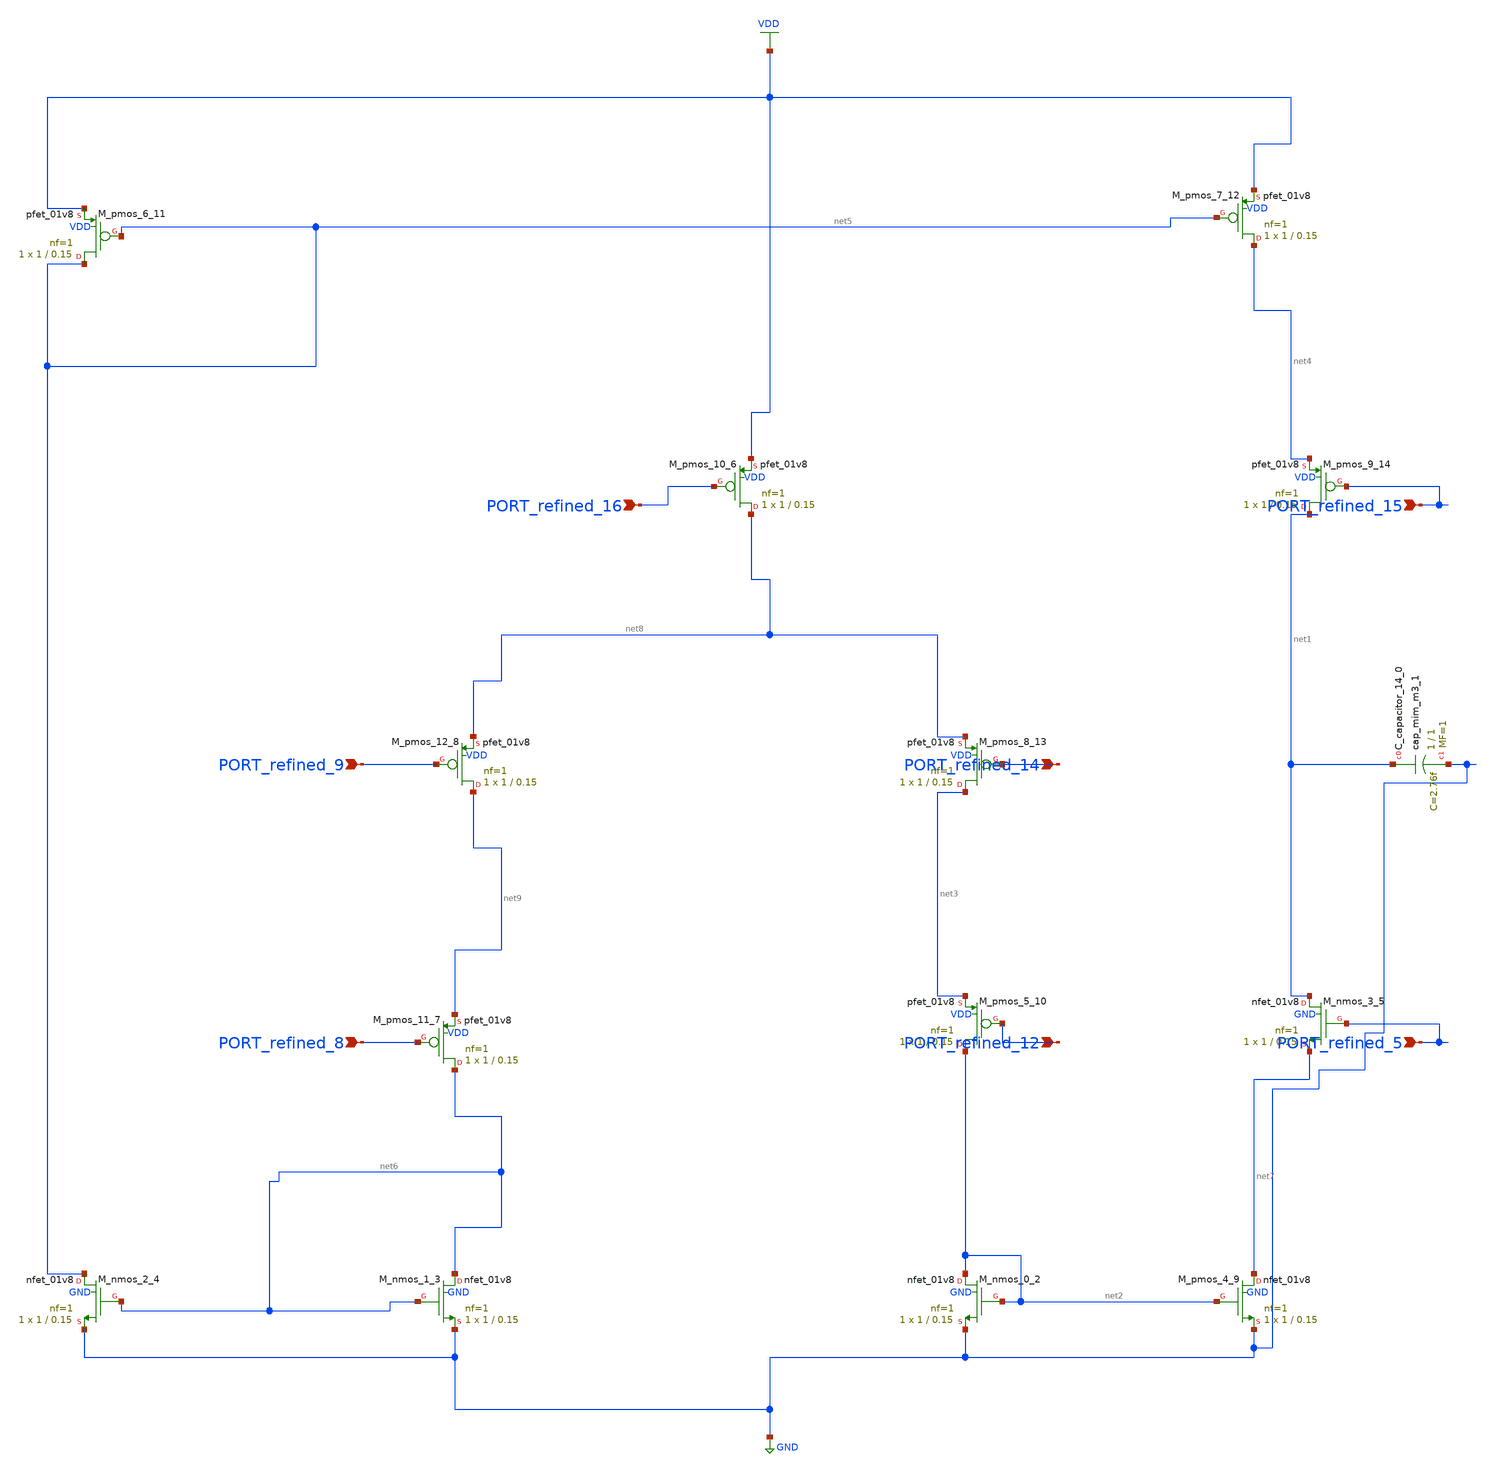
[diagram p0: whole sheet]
** sch_path: schematics/Image2Net/084.sch
**.subckt 084 PORT_refined_5 PORT_refined_9 PORT_refined_15 PORT_refined_14 PORT_refined_8
*+ PORT_refined_12 PORT_refined_16
*.ipin PORT_refined_5
*.ipin PORT_refined_9
*.ipin PORT_refined_15
*.ipin PORT_refined_14
*.ipin PORT_refined_8
*.ipin PORT_refined_12
*.ipin PORT_refined_16
XC_capacitor_14_0 net1 GND sky130_fd_pr__cap_mim_m3_1 W=1 L=1 MF=1 m=1
XM_nmos_0_2 net2 net2 GND GND sky130_fd_pr__nfet_01v8 L=0.15 W=1 nf=1 ad='int((1 + 1)/2) * 1 / 1 * 0.29'
+ as='int((1 + 2)/2) * 1 / 1 * 0.29' pd='2*int((1 + 1)/2) * (1 / 1 + 0.29)' ps='2*int((1 + 2)/2) * (1 / 1 + 0.29)'
+ nrd='0.29 / 1 ' nrs='0.29 / 1 ' sa=0 sb=0 sd=0 mult=1 m=1
XM_nmos_1_3 net6 net6 GND GND sky130_fd_pr__nfet_01v8 L=0.15 W=1 nf=1 ad='int((1 + 1)/2) * 1 / 1 * 0.29'
+ as='int((1 + 2)/2) * 1 / 1 * 0.29' pd='2*int((1 + 1)/2) * (1 / 1 + 0.29)' ps='2*int((1 + 2)/2) * (1 / 1 + 0.29)'
+ nrd='0.29 / 1 ' nrs='0.29 / 1 ' sa=0 sb=0 sd=0 mult=1 m=1
XM_nmos_2_4 net5 net6 GND GND sky130_fd_pr__nfet_01v8 L=0.15 W=1 nf=1 ad='int((1 + 1)/2) * 1 / 1 * 0.29'
+ as='int((1 + 2)/2) * 1 / 1 * 0.29' pd='2*int((1 + 1)/2) * (1 / 1 + 0.29)' ps='2*int((1 + 2)/2) * (1 / 1 + 0.29)'
+ nrd='0.29 / 1 ' nrs='0.29 / 1 ' sa=0 sb=0 sd=0 mult=1 m=1
XM_nmos_3_5 net1 PORT_refined_5 net7 GND sky130_fd_pr__nfet_01v8 L=0.15 W=1 nf=1 ad='int((1 + 1)/2) * 1 / 1 * 0.29'
+ as='int((1 + 2)/2) * 1 / 1 * 0.29' pd='2*int((1 + 1)/2) * (1 / 1 + 0.29)' ps='2*int((1 + 2)/2) * (1 / 1 + 0.29)'
+ nrd='0.29 / 1 ' nrs='0.29 / 1 ' sa=0 sb=0 sd=0 mult=1 m=1
XM_pmos_10_6 net8 PORT_refined_16 VDD VDD sky130_fd_pr__pfet_01v8 L=0.15 W=1 nf=1 ad='int((1 + 1)/2) * 1 / 1 * 0.29'
+ as='int((1 + 2)/2) * 1 / 1 * 0.29' pd='2*int((1 + 1)/2) * (1 / 1 + 0.29)' ps='2*int((1 + 2)/2) * (1 / 1 + 0.29)'
+ nrd='0.29 / 1 ' nrs='0.29 / 1 ' sa=0 sb=0 sd=0 mult=1 m=1
XM_pmos_11_7 net6 PORT_refined_8 net9 VDD sky130_fd_pr__pfet_01v8 L=0.15 W=1 nf=1 ad='int((1 + 1)/2) * 1 / 1 * 0.29'
+ as='int((1 + 2)/2) * 1 / 1 * 0.29' pd='2*int((1 + 1)/2) * (1 / 1 + 0.29)' ps='2*int((1 + 2)/2) * (1 / 1 + 0.29)'
+ nrd='0.29 / 1 ' nrs='0.29 / 1 ' sa=0 sb=0 sd=0 mult=1 m=1
XM_pmos_12_8 net9 PORT_refined_9 net8 VDD sky130_fd_pr__pfet_01v8 L=0.15 W=1 nf=1 ad='int((1 + 1)/2) * 1 / 1 * 0.29'
+ as='int((1 + 2)/2) * 1 / 1 * 0.29' pd='2*int((1 + 1)/2) * (1 / 1 + 0.29)' ps='2*int((1 + 2)/2) * (1 / 1 + 0.29)'
+ nrd='0.29 / 1 ' nrs='0.29 / 1 ' sa=0 sb=0 sd=0 mult=1 m=1
XM_pmos_4_9 net7 net2 GND GND sky130_fd_pr__nfet_01v8 L=0.15 W=1 nf=1 ad='int((1 + 1)/2) * 1 / 1 * 0.29'
+ as='int((1 + 2)/2) * 1 / 1 * 0.29' pd='2*int((1 + 1)/2) * (1 / 1 + 0.29)' ps='2*int((1 + 2)/2) * (1 / 1 + 0.29)'
+ nrd='0.29 / 1 ' nrs='0.29 / 1 ' sa=0 sb=0 sd=0 mult=1 m=1
XM_pmos_5_10 net2 PORT_refined_12 net3 VDD sky130_fd_pr__pfet_01v8 L=0.15 W=1 nf=1 ad='int((1 + 1)/2) * 1 / 1 * 0.29'
+ as='int((1 + 2)/2) * 1 / 1 * 0.29' pd='2*int((1 + 1)/2) * (1 / 1 + 0.29)' ps='2*int((1 + 2)/2) * (1 / 1 + 0.29)'
+ nrd='0.29 / 1 ' nrs='0.29 / 1 ' sa=0 sb=0 sd=0 mult=1 m=1
XM_pmos_6_11 net5 net5 VDD VDD sky130_fd_pr__pfet_01v8 L=0.15 W=1 nf=1 ad='int((1 + 1)/2) * 1 / 1 * 0.29'
+ as='int((1 + 2)/2) * 1 / 1 * 0.29' pd='2*int((1 + 1)/2) * (1 / 1 + 0.29)' ps='2*int((1 + 2)/2) * (1 / 1 + 0.29)'
+ nrd='0.29 / 1 ' nrs='0.29 / 1 ' sa=0 sb=0 sd=0 mult=1 m=1
XM_pmos_7_12 net4 net5 VDD VDD sky130_fd_pr__pfet_01v8 L=0.15 W=1 nf=1 ad='int((1 + 1)/2) * 1 / 1 * 0.29'
+ as='int((1 + 2)/2) * 1 / 1 * 0.29' pd='2*int((1 + 1)/2) * (1 / 1 + 0.29)' ps='2*int((1 + 2)/2) * (1 / 1 + 0.29)'
+ nrd='0.29 / 1 ' nrs='0.29 / 1 ' sa=0 sb=0 sd=0 mult=1 m=1
XM_pmos_8_13 net3 PORT_refined_14 net8 VDD sky130_fd_pr__pfet_01v8 L=0.15 W=1 nf=1 ad='int((1 + 1)/2) * 1 / 1 * 0.29'
+ as='int((1 + 2)/2) * 1 / 1 * 0.29' pd='2*int((1 + 1)/2) * (1 / 1 + 0.29)' ps='2*int((1 + 2)/2) * (1 / 1 + 0.29)'
+ nrd='0.29 / 1 ' nrs='0.29 / 1 ' sa=0 sb=0 sd=0 mult=1 m=1
XM_pmos_9_14 net1 PORT_refined_15 net4 VDD sky130_fd_pr__pfet_01v8 L=0.15 W=1 nf=1 ad='int((1 + 1)/2) * 1 / 1 * 0.29'
+ as='int((1 + 2)/2) * 1 / 1 * 0.29' pd='2*int((1 + 1)/2) * (1 / 1 + 0.29)' ps='2*int((1 + 2)/2) * (1 / 1 + 0.29)'
+ nrd='0.29 / 1 ' nrs='0.29 / 1 ' sa=0 sb=0 sd=0 mult=1 m=1
**.ends
.GLOBAL GND
.GLOBAL VDD
.end
